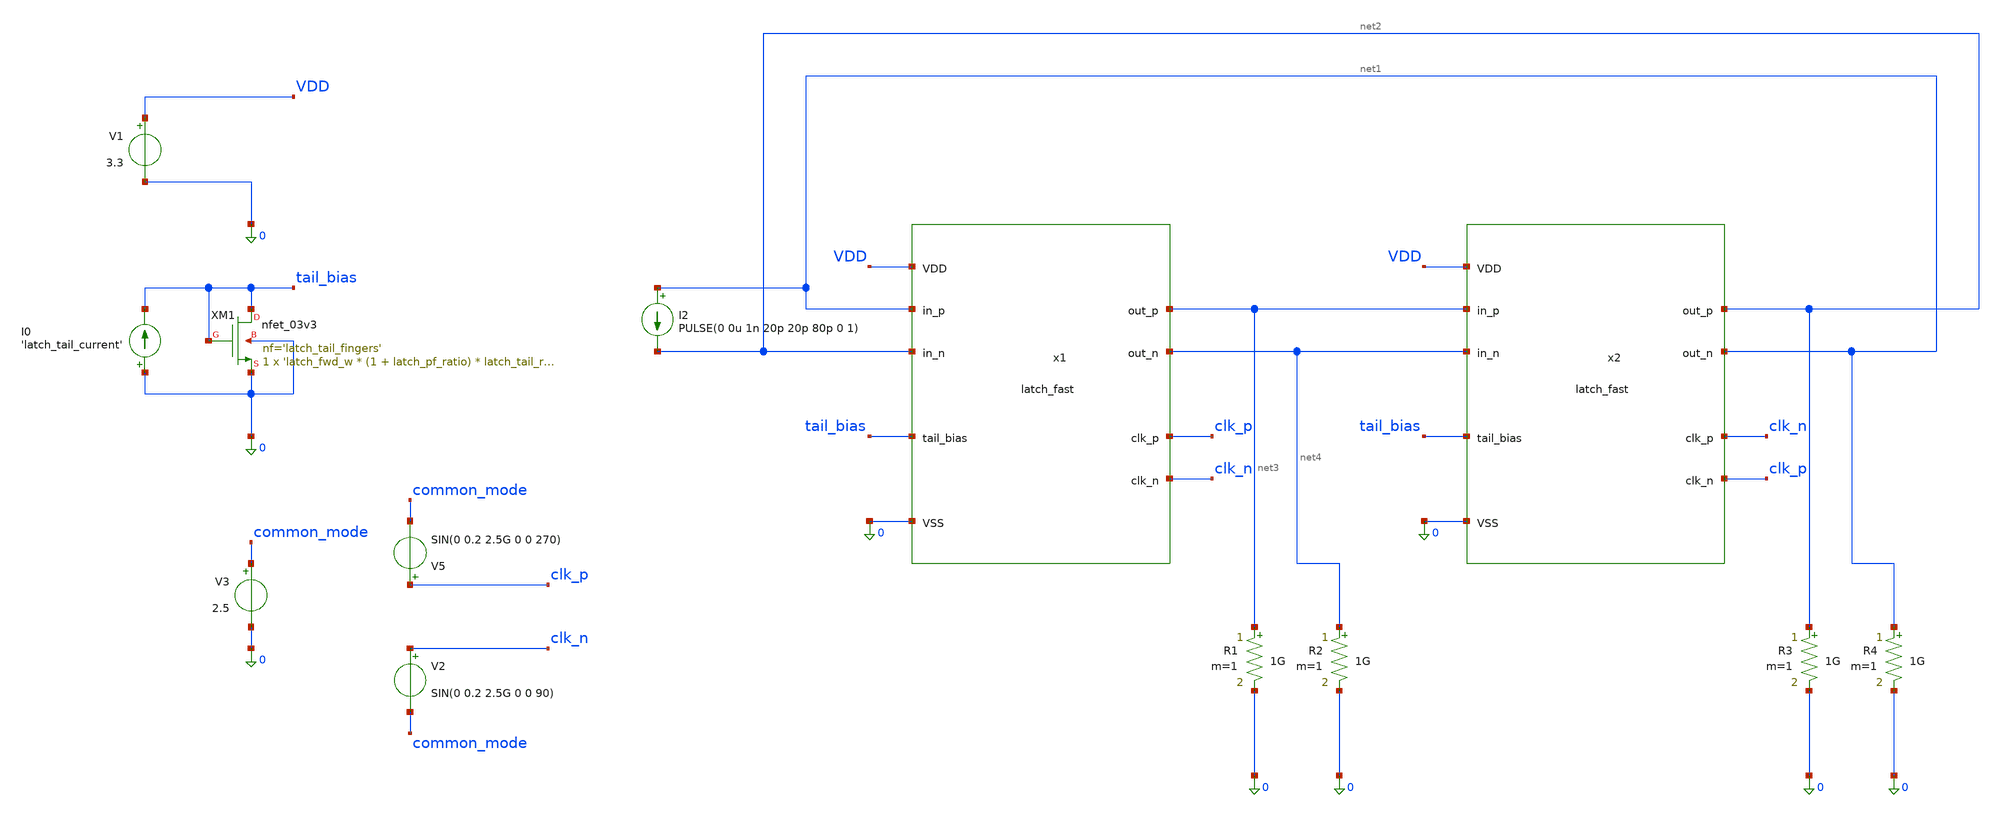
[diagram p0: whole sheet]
** sch_path: xschem/div2_tb.sch
**.subckt div2_tb
x1 0 VDD net4 net3 net1 net2 clk_n clk_p tail_bias latch_fast
XM1 tail_bias tail_bias 0 0 nfet_03v3 L='latch_tail_l' W='latch_fwd_w * (1 + latch_pf_ratio) * latch_tail_ratio'
+ nf='latch_tail_fingers' ad='int((nf+1)/2) * W/nf * 0.18u' as='int((nf+2)/2) * W/nf * 0.18u' pd='2*int((nf+1)/2) * (W/nf + 0.18u)'
+ ps='2*int((nf+2)/2) * (W/nf + 0.18u)' nrd='0.18u / W' nrs='0.18u / W' sa=0 sb=0 sd=0 m=1
x2 0 VDD net1 net2 net3 net4 clk_p clk_n tail_bias latch_fast
V1 VDD 0 3.3
I0 0 tail_bias 'latch_tail_current'
I2 net1 net2 PULSE(0 0u 1n 20p 20p 80p 0 1)
R1 net3 0 1G m=1
R2 net4 0 1G m=1
R3 net2 0 1G m=1
R4 net1 0 1G m=1
V2 clk_n common_mode SIN(0 0.2 2.5G 0 0 90)
V5 clk_p common_mode SIN(0 0.2 2.5G 0 0 270)
V3 common_mode 0 2.5
**** begin user architecture code
 .include $::180MCU_MODELS/design.ngspice
.lib $::180MCU_MODELS/sm141064.ngspice typical
.lib $::180MCU_MODELS/sm141064.ngspice res_typical


.option savecurrents

.param latch_fwd_w=2u
.param latch_pf_ratio='1'
.param latch_fwd_fingers=1
.param latch_pf_fingers=1
.param latch_tail_fingers=20
.param latch_clk_ratio=0.5
.param latch_clk_fingers=1
.param latch_tail_ratio=10
.param latch_tail_l=1u
.param latch_load_w=1u
.param latch_load_r=12k
.param latch_load_l='latch_load_r/1000 * latch_load_w'
.param latch_tail_current=64u

.nodeset v(net1)=2.5

.control
save all
tran 5p 50n
plot clk_p clk_n net1 net2 net3 net4 x1.net1
.endc
**** end user architecture code
**.ends

* expanding   symbol:  latch_fast.sym # of pins=9
** sym_path: xschem/latch_fast.sym
** sch_path: xschem/latch_fast.sch
.subckt latch_fast VSS VDD out_n out_p in_p in_n clk_n clk_p tail_bias
*.ipin VSS
*.ipin VDD
*.opin out_n
*.opin out_p
*.ipin in_p
*.ipin in_n
*.ipin clk_p
*.ipin clk_n
*.ipin tail_bias
XM1 out_n in_p net2 VSS nfet_03v3 L=0.28u W='latch_fwd_w' nf='latch_fwd_fingers' ad='int((nf+1)/2) * W/nf * 0.18u'
+ as='int((nf+2)/2) * W/nf * 0.18u' pd='2*int((nf+1)/2) * (W/nf + 0.18u)' ps='2*int((nf+2)/2) * (W/nf + 0.18u)'
+ nrd='0.18u / W' nrs='0.18u / W' sa=0 sb=0 sd=0 m=1
XM3 out_n out_p net3 VSS nfet_03v3 L=0.28u W='latch_fwd_w * latch_pf_ratio' nf='latch_pf_fingers' ad='int((nf+1)/2) * W/nf * 0.18u'
+ as='int((nf+2)/2) * W/nf * 0.18u' pd='2*int((nf+1)/2) * (W/nf + 0.18u)' ps='2*int((nf+2)/2) * (W/nf + 0.18u)'
+ nrd='0.18u / W' nrs='0.18u / W' sa=0 sb=0 sd=0 m=1
XM4 out_p out_n net3 VSS nfet_03v3 L=0.28u W='latch_fwd_w * latch_pf_ratio' nf='latch_pf_fingers' ad='int((nf+1)/2) * W/nf * 0.18u'
+ as='int((nf+2)/2) * W/nf * 0.18u' pd='2*int((nf+1)/2) * (W/nf + 0.18u)' ps='2*int((nf+2)/2) * (W/nf + 0.18u)'
+ nrd='0.18u / W' nrs='0.18u / W' sa=0 sb=0 sd=0 m=1
XM5 net1 tail_bias VSS VSS nfet_03v3 L='latch_tail_l' W={latch_fwd_w * (1 + latch_pf_ratio) * latch_tail_ratio}
+ nf='latch_tail_fingers' ad='int((nf+1)/2) * W/nf * 0.18u' as='int((nf+2)/2) * W/nf * 0.18u' pd='2*int((nf+1)/2) * (W/nf + 0.18u)'
+ ps='2*int((nf+2)/2) * (W/nf + 0.18u)' nrd='0.18u / W' nrs='0.18u / W' sa=0 sb=0 sd=0 m=1
XM2 out_p in_n net2 VSS nfet_03v3 L=0.28u W='latch_fwd_w' nf='latch_fwd_fingers' ad='int((nf+1)/2) * W/nf * 0.18u'
+ as='int((nf+2)/2) * W/nf * 0.18u' pd='2*int((nf+1)/2) * (W/nf + 0.18u)' ps='2*int((nf+2)/2) * (W/nf + 0.18u)'
+ nrd='0.18u / W' nrs='0.18u / W' sa=0 sb=0 sd=0 m=1
XR1 out_n VDD VSS ppolyf_u_1k r_width='latch_load_w' r_length='latch_load_l' m=1
XR2 out_p VDD VSS ppolyf_u_1k r_width='latch_load_w' r_length='latch_load_l' m=1
XM6 net2 clk_p net1 VSS nfet_03v3 L=0.28u W='latch_fwd_w * latch_clk_ratio' nf='latch_clk_fingers' ad='int((nf+1)/2) * W/nf * 0.18u'
+ as='int((nf+2)/2) * W/nf * 0.18u' pd='2*int((nf+1)/2) * (W/nf + 0.18u)' ps='2*int((nf+2)/2) * (W/nf + 0.18u)'
+ nrd='0.18u / W' nrs='0.18u / W' sa=0 sb=0 sd=0 m=1
XM7 net3 clk_n net1 VSS nfet_03v3 L=0.28u W='latch_fwd_w * latch_clk_ratio' nf='latch_clk_fingers' ad='int((nf+1)/2) * W/nf * 0.18u'
+ as='int((nf+2)/2) * W/nf * 0.18u' pd='2*int((nf+1)/2) * (W/nf + 0.18u)' ps='2*int((nf+2)/2) * (W/nf + 0.18u)'
+ nrd='0.18u / W' nrs='0.18u / W' sa=0 sb=0 sd=0 m=1
.ends

.end
